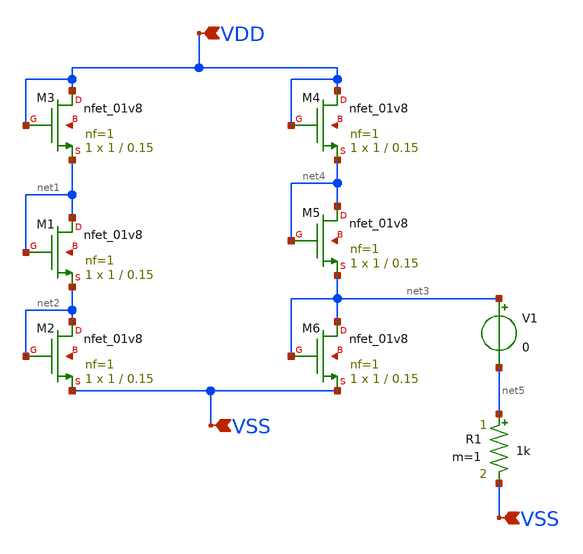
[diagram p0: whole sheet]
** sch_path: design/RPLY_EXTEMP0_SKY130NM/EXTEMP0.sch
**.subckt EXTEMP0 VDD VSS VSS
*.ipin VDD
*.ipin VSS
*.ipin VSS
XM1 net1 net1 net2 net6 sky130_fd_pr__nfet_01v8 L=0.15 W=1 nf=1 ad='int((nf+1)/2) * W/nf * 0.29' as='int((nf+2)/2) * W/nf * 0.29'
+ pd='2*int((nf+1)/2) * (W/nf + 0.29)' ps='2*int((nf+2)/2) * (W/nf + 0.29)' nrd='0.29 / W' nrs='0.29 / W'
+ sa=0 sb=0 sd=0 mult=1 m=1
XM2 net2 net2 VSS net7 sky130_fd_pr__nfet_01v8 L=0.15 W=1 nf=1 ad='int((nf+1)/2) * W/nf * 0.29' as='int((nf+2)/2) * W/nf * 0.29'
+ pd='2*int((nf+1)/2) * (W/nf + 0.29)' ps='2*int((nf+2)/2) * (W/nf + 0.29)' nrd='0.29 / W' nrs='0.29 / W'
+ sa=0 sb=0 sd=0 mult=1 m=1
XM3 VDD VDD net1 net8 sky130_fd_pr__nfet_01v8 L=0.15 W=1 nf=1 ad='int((nf+1)/2) * W/nf * 0.29' as='int((nf+2)/2) * W/nf * 0.29'
+ pd='2*int((nf+1)/2) * (W/nf + 0.29)' ps='2*int((nf+2)/2) * (W/nf + 0.29)' nrd='0.29 / W' nrs='0.29 / W'
+ sa=0 sb=0 sd=0 mult=1 m=1
XM4 VDD VDD net4 net9 sky130_fd_pr__nfet_01v8 L=0.15 W=1 nf=1 ad='int((nf+1)/2) * W/nf * 0.29' as='int((nf+2)/2) * W/nf * 0.29'
+ pd='2*int((nf+1)/2) * (W/nf + 0.29)' ps='2*int((nf+2)/2) * (W/nf + 0.29)' nrd='0.29 / W' nrs='0.29 / W'
+ sa=0 sb=0 sd=0 mult=1 m=1
XM5 net4 net4 net3 net10 sky130_fd_pr__nfet_01v8 L=0.15 W=1 nf=1 ad='int((nf+1)/2) * W/nf * 0.29' as='int((nf+2)/2) * W/nf * 0.29'
+ pd='2*int((nf+1)/2) * (W/nf + 0.29)' ps='2*int((nf+2)/2) * (W/nf + 0.29)' nrd='0.29 / W' nrs='0.29 / W'
+ sa=0 sb=0 sd=0 mult=1 m=1
XM6 net3 net3 VSS net11 sky130_fd_pr__nfet_01v8 L=0.15 W=1 nf=1 ad='int((nf+1)/2) * W/nf * 0.29' as='int((nf+2)/2) * W/nf * 0.29'
+ pd='2*int((nf+1)/2) * (W/nf + 0.29)' ps='2*int((nf+2)/2) * (W/nf + 0.29)' nrd='0.29 / W' nrs='0.29 / W'
+ sa=0 sb=0 sd=0 mult=1 m=1
R1 net5 VSS 1k m=1
V1 net3 net5 0
**.ends
.end
